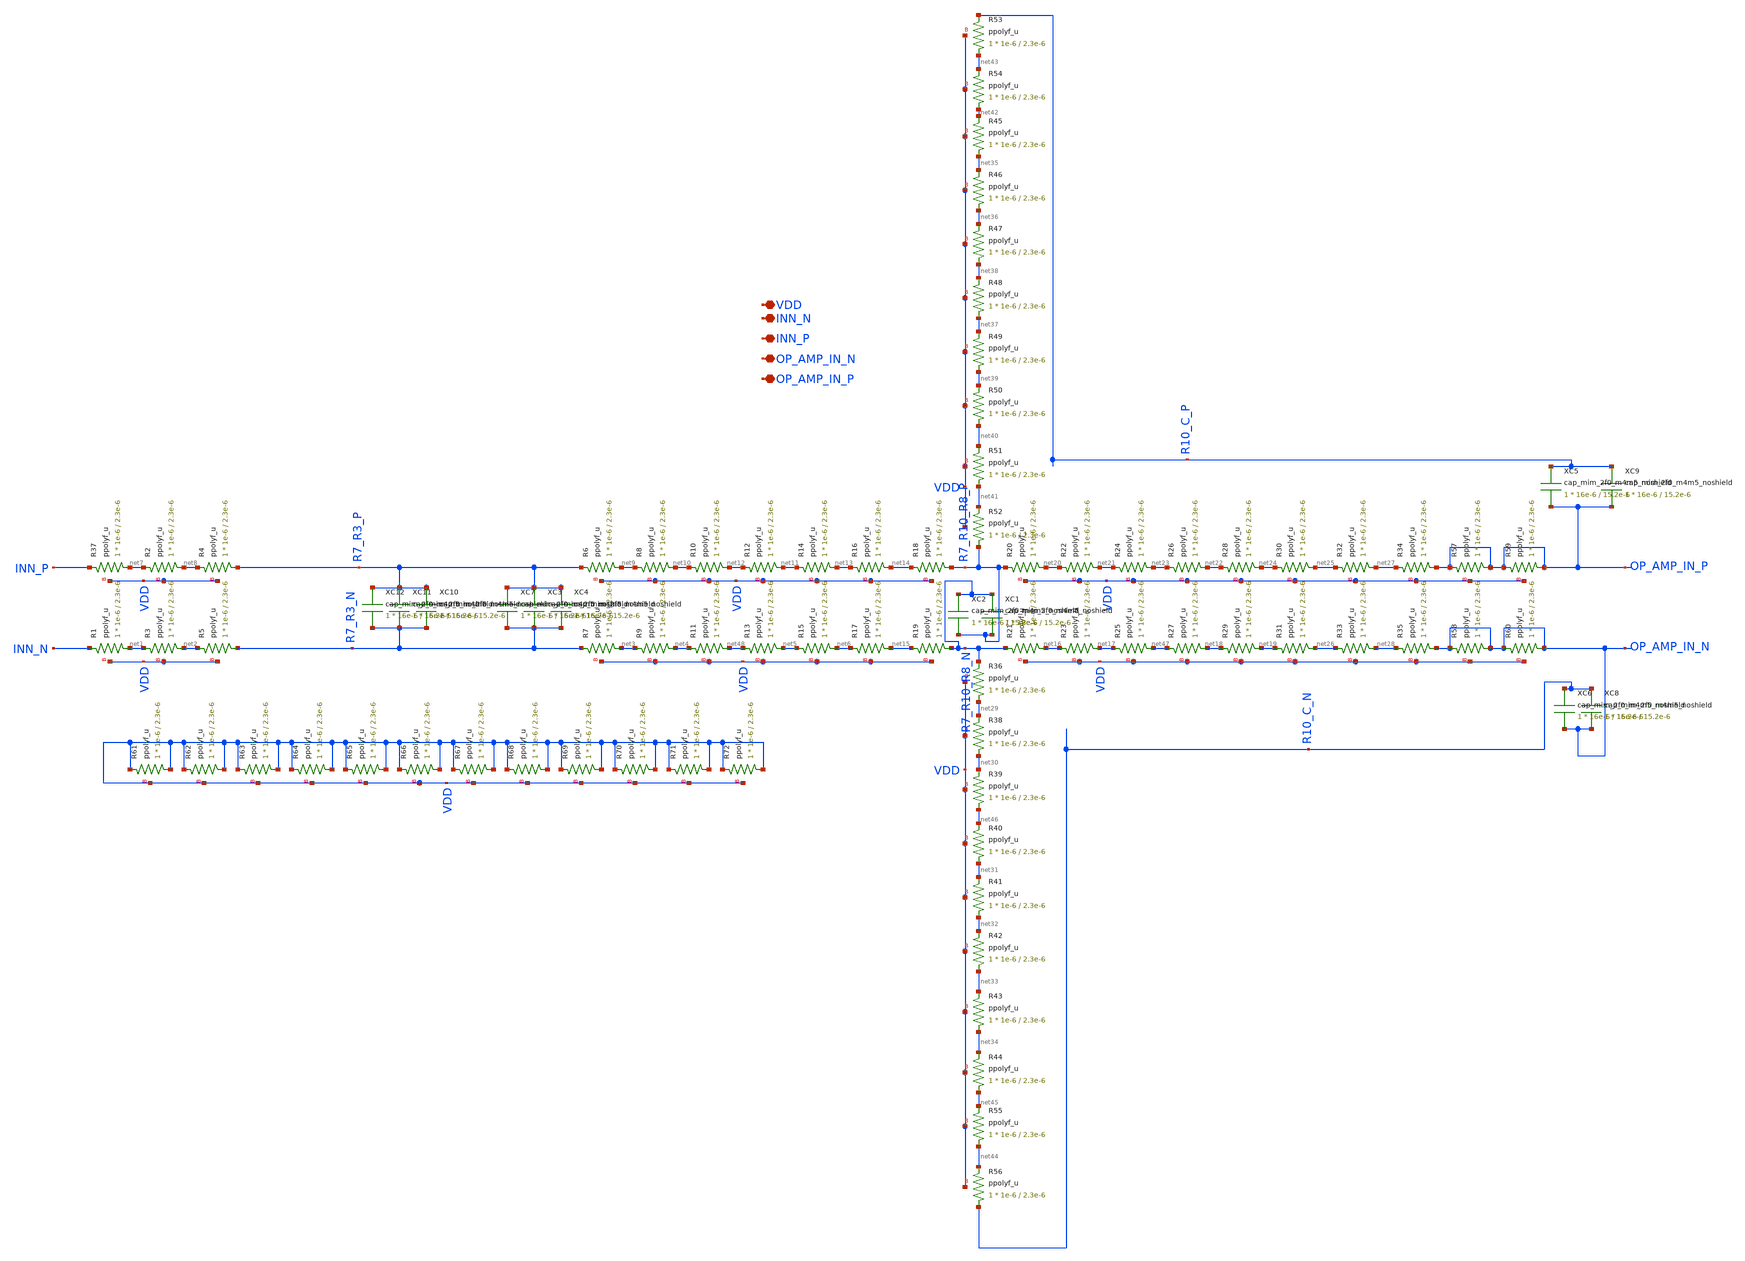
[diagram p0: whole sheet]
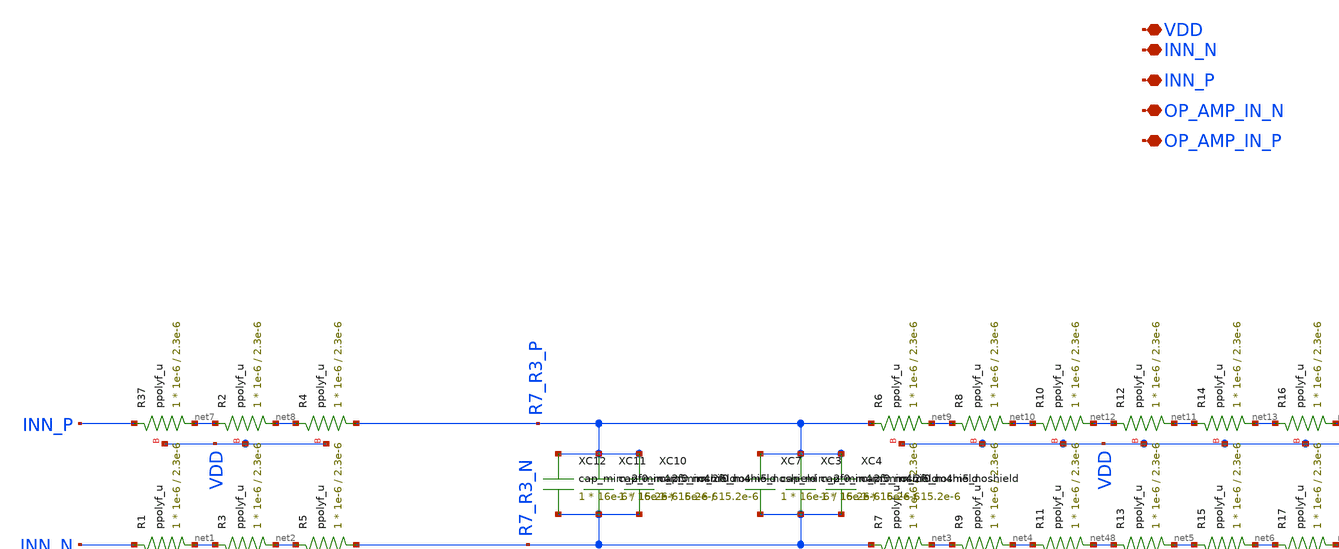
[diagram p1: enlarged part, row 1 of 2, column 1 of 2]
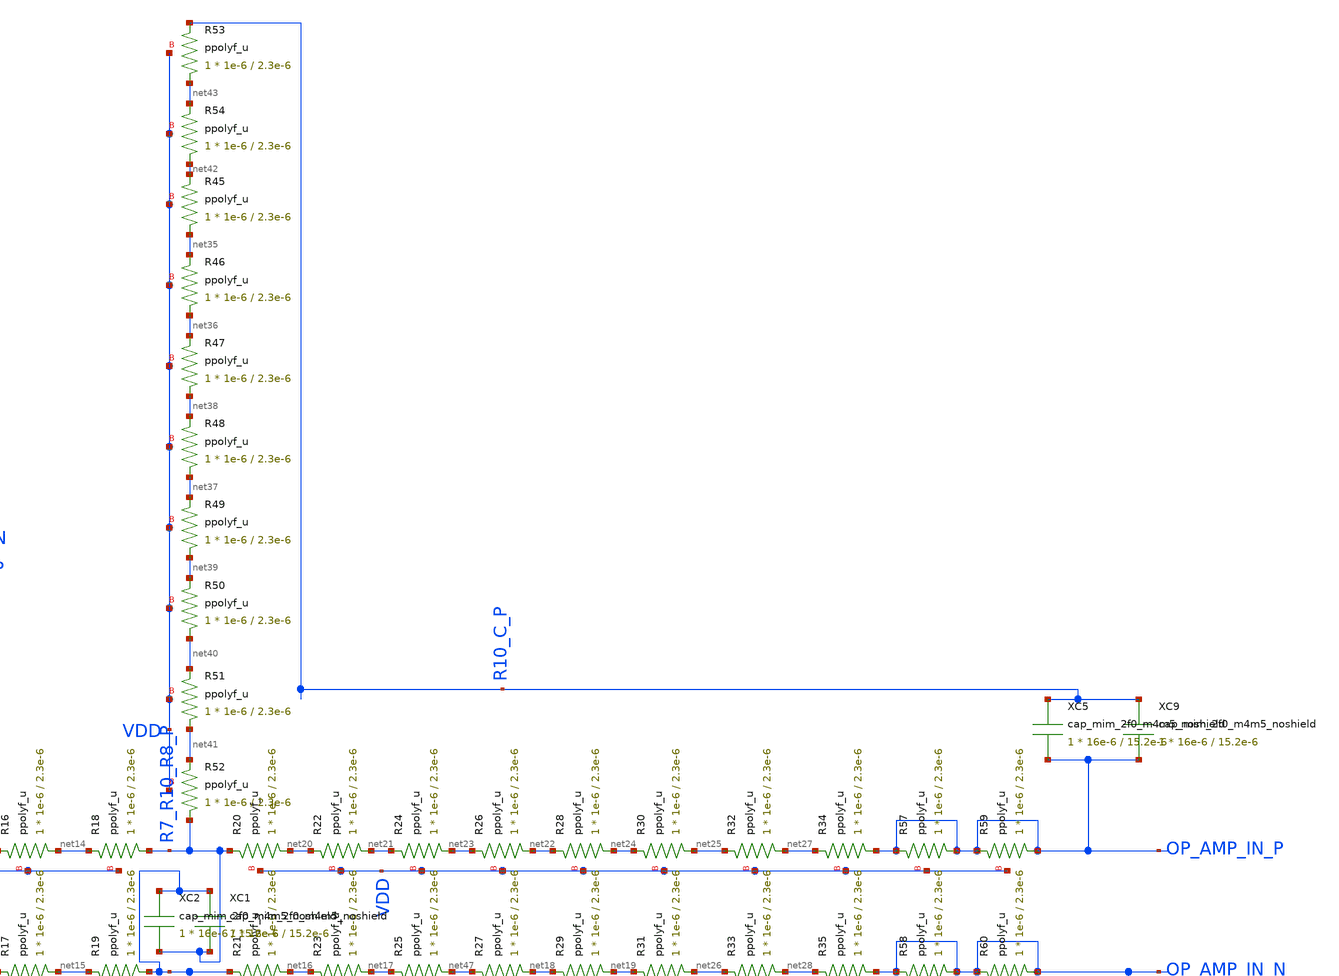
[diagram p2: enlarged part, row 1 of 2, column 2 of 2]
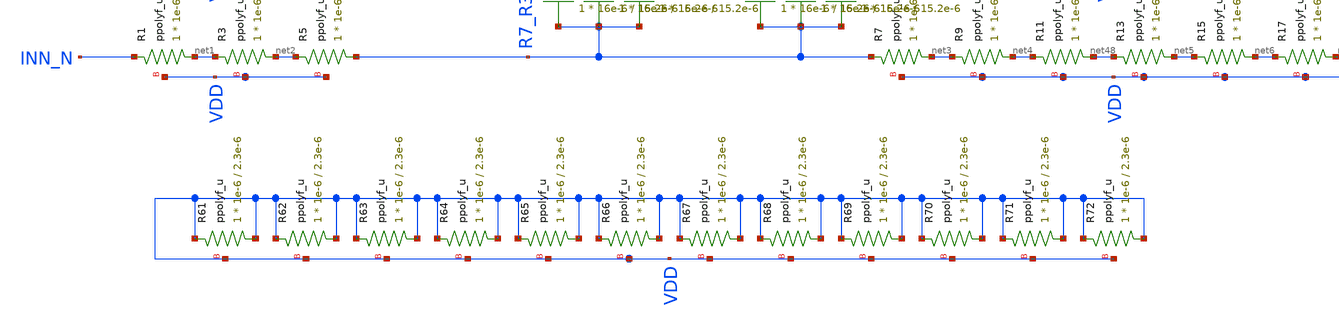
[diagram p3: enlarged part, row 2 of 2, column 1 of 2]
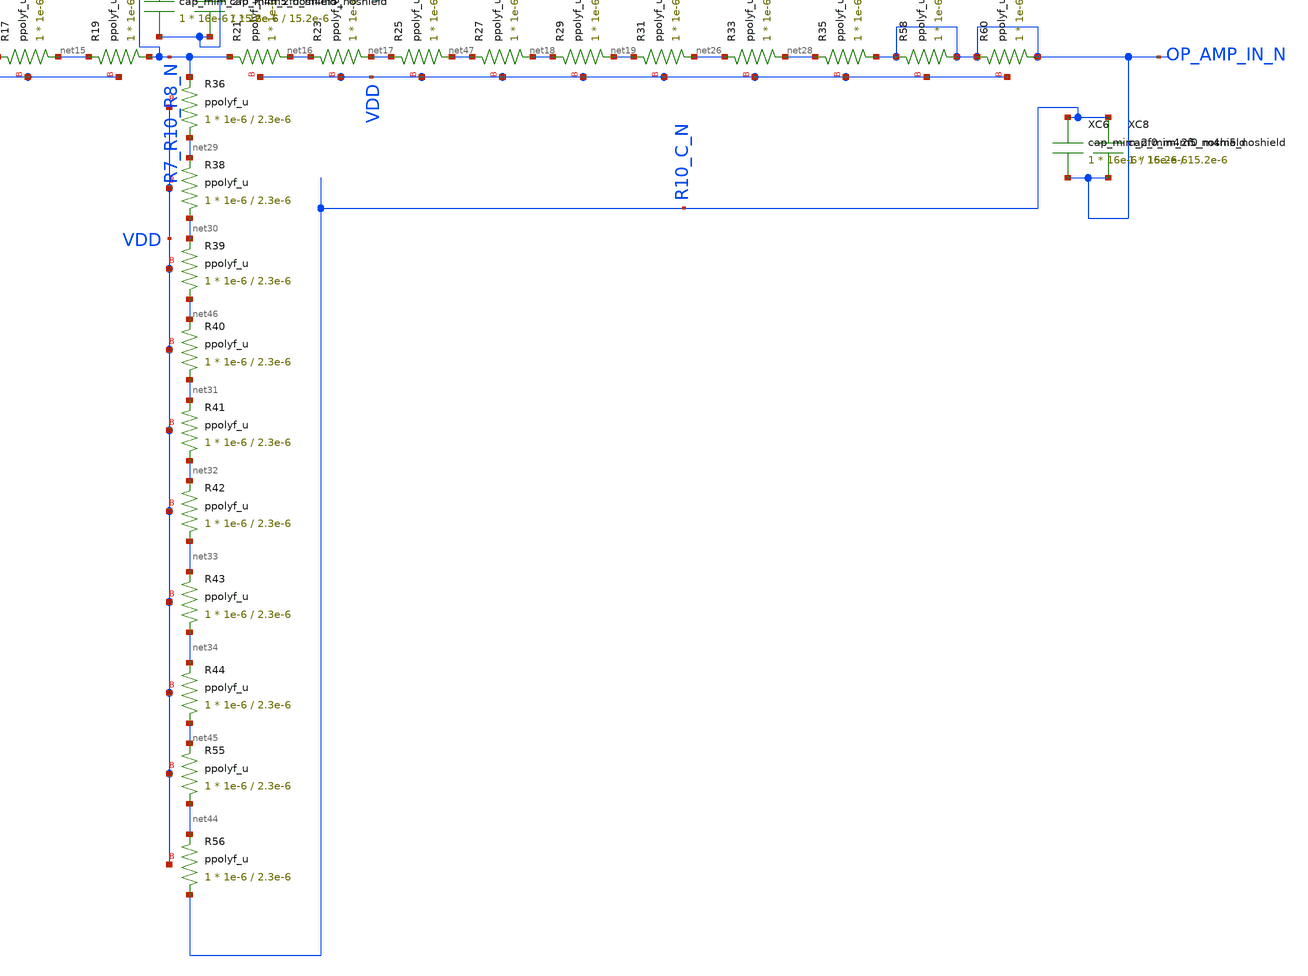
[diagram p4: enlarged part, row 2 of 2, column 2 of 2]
** sch_path: AWG_OUTPUT_AND_MUX_PAKISTAN_05/xschem/filter_res.sch
**.subckt filter_res VDD INN_N OP_AMP_IN_N INN_P OP_AMP_IN_P
*.iopin VDD
*.iopin INN_N
*.iopin OP_AMP_IN_N
*.iopin INN_P
*.iopin OP_AMP_IN_P
XR37 net7 INN_P VDD ppolyf_u r_width=1e-6 r_length=2.3e-6 m=1
XR1 net1 INN_N VDD ppolyf_u r_width=1e-6 r_length=2.3e-6 m=1
XR2 net8 net7 VDD ppolyf_u r_width=1e-6 r_length=2.3e-6 m=1
XR3 net2 net1 VDD ppolyf_u r_width=1e-6 r_length=2.3e-6 m=1
XR4 R7_R3_P net8 VDD ppolyf_u r_width=1e-6 r_length=2.3e-6 m=1
XR5 R7_R3_N net2 VDD ppolyf_u r_width=1e-6 r_length=2.3e-6 m=1
XR6 net9 R7_R3_P VDD ppolyf_u r_width=1e-6 r_length=2.3e-6 m=1
XR7 net3 R7_R3_N VDD ppolyf_u r_width=1e-6 r_length=2.3e-6 m=1
XR8 net10 net9 VDD ppolyf_u r_width=1e-6 r_length=2.3e-6 m=1
XR9 net4 net3 VDD ppolyf_u r_width=1e-6 r_length=2.3e-6 m=1
XR10 net12 net10 VDD ppolyf_u r_width=1e-6 r_length=2.3e-6 m=1
XR11 net48 net4 VDD ppolyf_u r_width=1e-6 r_length=2.3e-6 m=1
XR12 net11 net12 VDD ppolyf_u r_width=1e-6 r_length=2.3e-6 m=1
XR13 net5 net48 VDD ppolyf_u r_width=1e-6 r_length=2.3e-6 m=1
XR14 net13 net11 VDD ppolyf_u r_width=1e-6 r_length=2.3e-6 m=1
XR15 net6 net5 VDD ppolyf_u r_width=1e-6 r_length=2.3e-6 m=1
XR16 net14 net13 VDD ppolyf_u r_width=1e-6 r_length=2.3e-6 m=1
XR17 net15 net6 VDD ppolyf_u r_width=1e-6 r_length=2.3e-6 m=1
XR18 R7_R10_R8_P net14 VDD ppolyf_u r_width=1e-6 r_length=2.3e-6 m=1
XR19 R7_R10_R8_N net15 VDD ppolyf_u r_width=1e-6 r_length=2.3e-6 m=1
XR20 net20 R7_R10_R8_P VDD ppolyf_u r_width=1e-6 r_length=2.3e-6 m=1
XR21 net16 R7_R10_R8_N VDD ppolyf_u r_width=1e-6 r_length=2.3e-6 m=1
XR22 net21 net20 VDD ppolyf_u r_width=1e-6 r_length=2.3e-6 m=1
XR23 net17 net16 VDD ppolyf_u r_width=1e-6 r_length=2.3e-6 m=1
XR24 net23 net21 VDD ppolyf_u r_width=1e-6 r_length=2.3e-6 m=1
XR25 net47 net17 VDD ppolyf_u r_width=1e-6 r_length=2.3e-6 m=1
XR26 net22 net23 VDD ppolyf_u r_width=1e-6 r_length=2.3e-6 m=1
XR27 net18 net47 VDD ppolyf_u r_width=1e-6 r_length=2.3e-6 m=1
XR28 net24 net22 VDD ppolyf_u r_width=1e-6 r_length=2.3e-6 m=1
XR29 net19 net18 VDD ppolyf_u r_width=1e-6 r_length=2.3e-6 m=1
XR30 net25 net24 VDD ppolyf_u r_width=1e-6 r_length=2.3e-6 m=1
XR31 net26 net19 VDD ppolyf_u r_width=1e-6 r_length=2.3e-6 m=1
XR32 net27 net25 VDD ppolyf_u r_width=1e-6 r_length=2.3e-6 m=1
XR33 net28 net26 VDD ppolyf_u r_width=1e-6 r_length=2.3e-6 m=1
XR34 OP_AMP_IN_P net27 VDD ppolyf_u r_width=1e-6 r_length=2.3e-6 m=1
XR35 OP_AMP_IN_N net28 VDD ppolyf_u r_width=1e-6 r_length=2.3e-6 m=1
XR36 net29 R7_R10_R8_N VDD ppolyf_u r_width=1e-6 r_length=2.3e-6 m=1
XR38 net30 net29 VDD ppolyf_u r_width=1e-6 r_length=2.3e-6 m=1
XR39 net46 net30 VDD ppolyf_u r_width=1e-6 r_length=2.3e-6 m=1
XR40 net31 net46 VDD ppolyf_u r_width=1e-6 r_length=2.3e-6 m=1
XR41 net32 net31 VDD ppolyf_u r_width=1e-6 r_length=2.3e-6 m=1
XR42 net33 net32 VDD ppolyf_u r_width=1e-6 r_length=2.3e-6 m=1
XR43 net34 net33 VDD ppolyf_u r_width=1e-6 r_length=2.3e-6 m=1
XR44 net45 net34 VDD ppolyf_u r_width=1e-6 r_length=2.3e-6 m=1
XR45 net35 net42 VDD ppolyf_u r_width=1e-6 r_length=2.3e-6 m=1
XR46 net36 net35 VDD ppolyf_u r_width=1e-6 r_length=2.3e-6 m=1
XR47 net38 net36 VDD ppolyf_u r_width=1e-6 r_length=2.3e-6 m=1
XR48 net37 net38 VDD ppolyf_u r_width=1e-6 r_length=2.3e-6 m=1
XR49 net39 net37 VDD ppolyf_u r_width=1e-6 r_length=2.3e-6 m=1
XR50 net40 net39 VDD ppolyf_u r_width=1e-6 r_length=2.3e-6 m=1
XR51 net41 net40 VDD ppolyf_u r_width=1e-6 r_length=2.3e-6 m=1
XR52 R7_R10_R8_P net41 VDD ppolyf_u r_width=1e-6 r_length=2.3e-6 m=1
XR53 net43 R10_C_P VDD ppolyf_u r_width=1e-6 r_length=2.3e-6 m=1
XR54 net42 net43 VDD ppolyf_u r_width=1e-6 r_length=2.3e-6 m=1
XR55 net44 net45 VDD ppolyf_u r_width=1e-6 r_length=2.3e-6 m=1
XR56 R10_C_N net44 VDD ppolyf_u r_width=1e-6 r_length=2.3e-6 m=1
XR57 OP_AMP_IN_P OP_AMP_IN_P VDD ppolyf_u r_width=1e-6 r_length=2.3e-6 m=1
XR58 OP_AMP_IN_N OP_AMP_IN_N VDD ppolyf_u r_width=1e-6 r_length=2.3e-6 m=1
XR59 OP_AMP_IN_P OP_AMP_IN_P VDD ppolyf_u r_width=1e-6 r_length=2.3e-6 m=1
XR60 OP_AMP_IN_N OP_AMP_IN_N VDD ppolyf_u r_width=1e-6 r_length=2.3e-6 m=1
XC5 R10_C_P OP_AMP_IN_P cap_mim_2f0_m4m5_noshield c_width=16e-6 c_length=15.2e-6 m=1
XC6 R10_C_N OP_AMP_IN_N cap_mim_2f0_m4m5_noshield c_width=16e-6 c_length=15.2e-6 m=1
XR61 VDD VDD VDD ppolyf_u r_width=1e-6 r_length=2.3e-6 m=1
XR62 VDD VDD VDD ppolyf_u r_width=1e-6 r_length=2.3e-6 m=1
XR63 VDD VDD VDD ppolyf_u r_width=1e-6 r_length=2.3e-6 m=1
XR64 VDD VDD VDD ppolyf_u r_width=1e-6 r_length=2.3e-6 m=1
XR65 VDD VDD VDD ppolyf_u r_width=1e-6 r_length=2.3e-6 m=1
XR66 VDD VDD VDD ppolyf_u r_width=1e-6 r_length=2.3e-6 m=1
XR67 VDD VDD VDD ppolyf_u r_width=1e-6 r_length=2.3e-6 m=1
XR68 VDD VDD VDD ppolyf_u r_width=1e-6 r_length=2.3e-6 m=1
XR69 VDD VDD VDD ppolyf_u r_width=1e-6 r_length=2.3e-6 m=1
XR70 VDD VDD VDD ppolyf_u r_width=1e-6 r_length=2.3e-6 m=1
XR71 VDD VDD VDD ppolyf_u r_width=1e-6 r_length=2.3e-6 m=1
XR72 VDD VDD VDD ppolyf_u r_width=1e-6 r_length=2.3e-6 m=1
XC8 R10_C_N OP_AMP_IN_N cap_mim_2f0_m4m5_noshield c_width=16e-6 c_length=15.2e-6 m=1
XC9 R10_C_P OP_AMP_IN_P cap_mim_2f0_m4m5_noshield c_width=16e-6 c_length=15.2e-6 m=1
XC1 R7_R10_R8_N R7_R10_R8_P cap_mim_2f0_m4m5_noshield c_width=16e-6 c_length=15.2e-6 m=1
XC2 R7_R10_R8_N R7_R10_R8_P cap_mim_2f0_m4m5_noshield c_width=16e-6 c_length=15.2e-6 m=1
XC3 R7_R3_P R7_R3_N cap_mim_2f0_m4m5_noshield c_width=16e-6 c_length=15.2e-6 m=1
XC4 R7_R3_P R7_R3_N cap_mim_2f0_m4m5_noshield c_width=16e-6 c_length=15.2e-6 m=1
XC7 R7_R3_P R7_R3_N cap_mim_2f0_m4m5_noshield c_width=16e-6 c_length=15.2e-6 m=1
XC10 R7_R3_P R7_R3_N cap_mim_2f0_m4m5_noshield c_width=16e-6 c_length=15.2e-6 m=1
XC11 R7_R3_P R7_R3_N cap_mim_2f0_m4m5_noshield c_width=16e-6 c_length=15.2e-6 m=1
XC12 R7_R3_P R7_R3_N cap_mim_2f0_m4m5_noshield c_width=16e-6 c_length=15.2e-6 m=1
**.ends
.end
